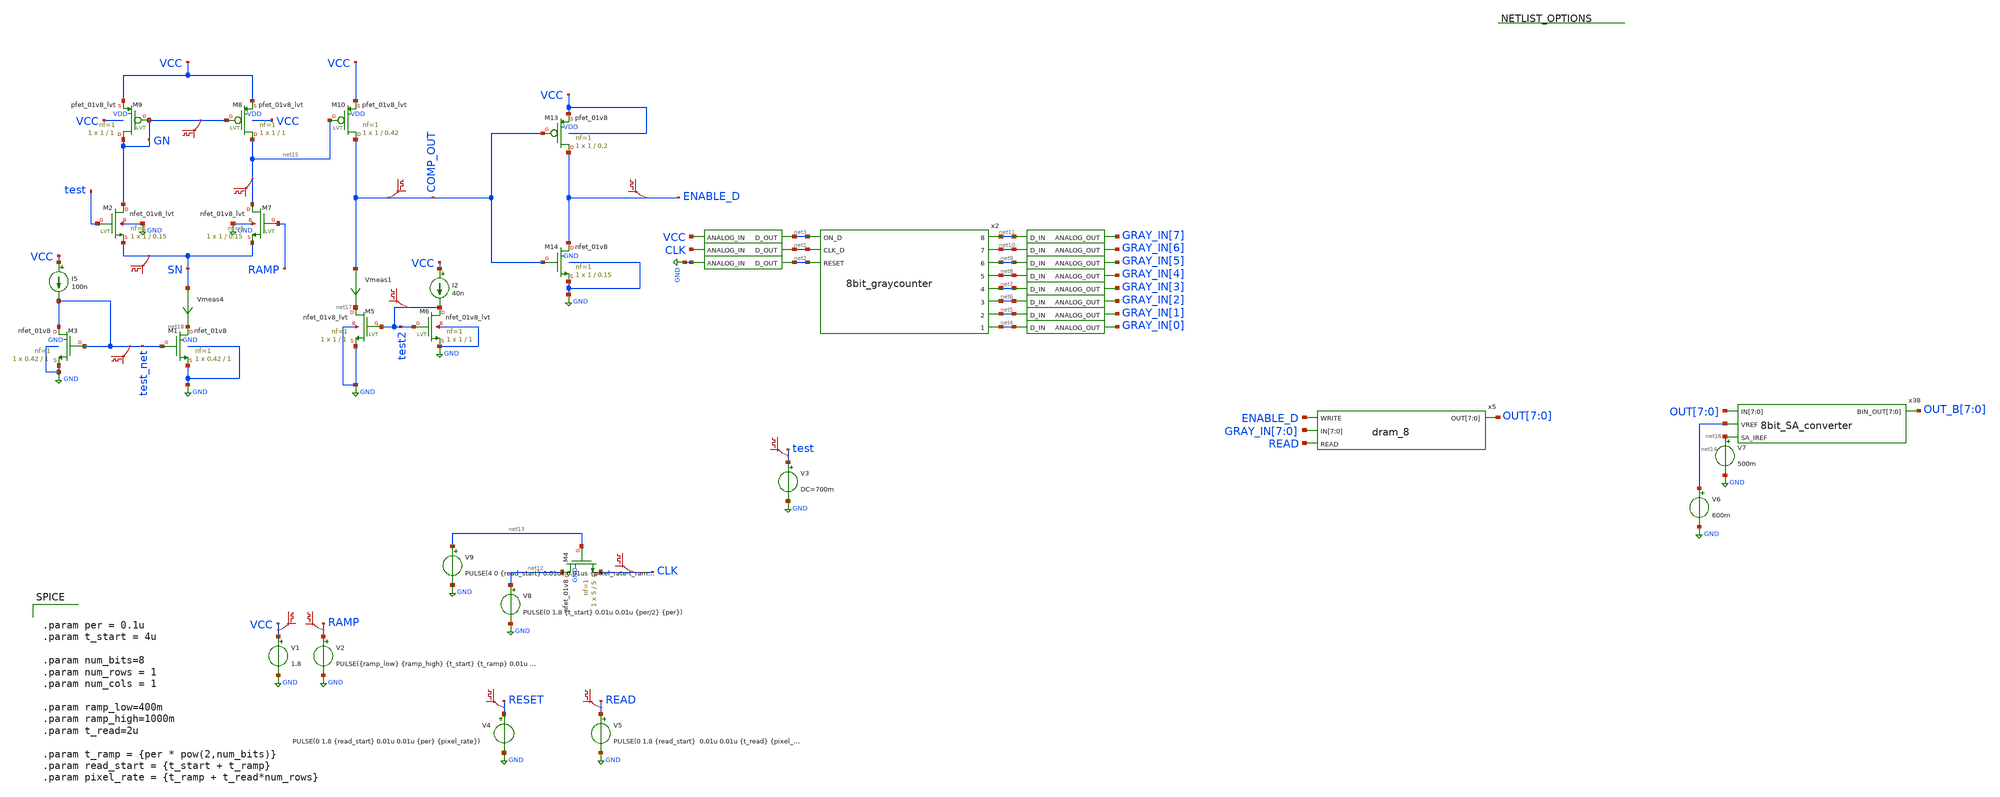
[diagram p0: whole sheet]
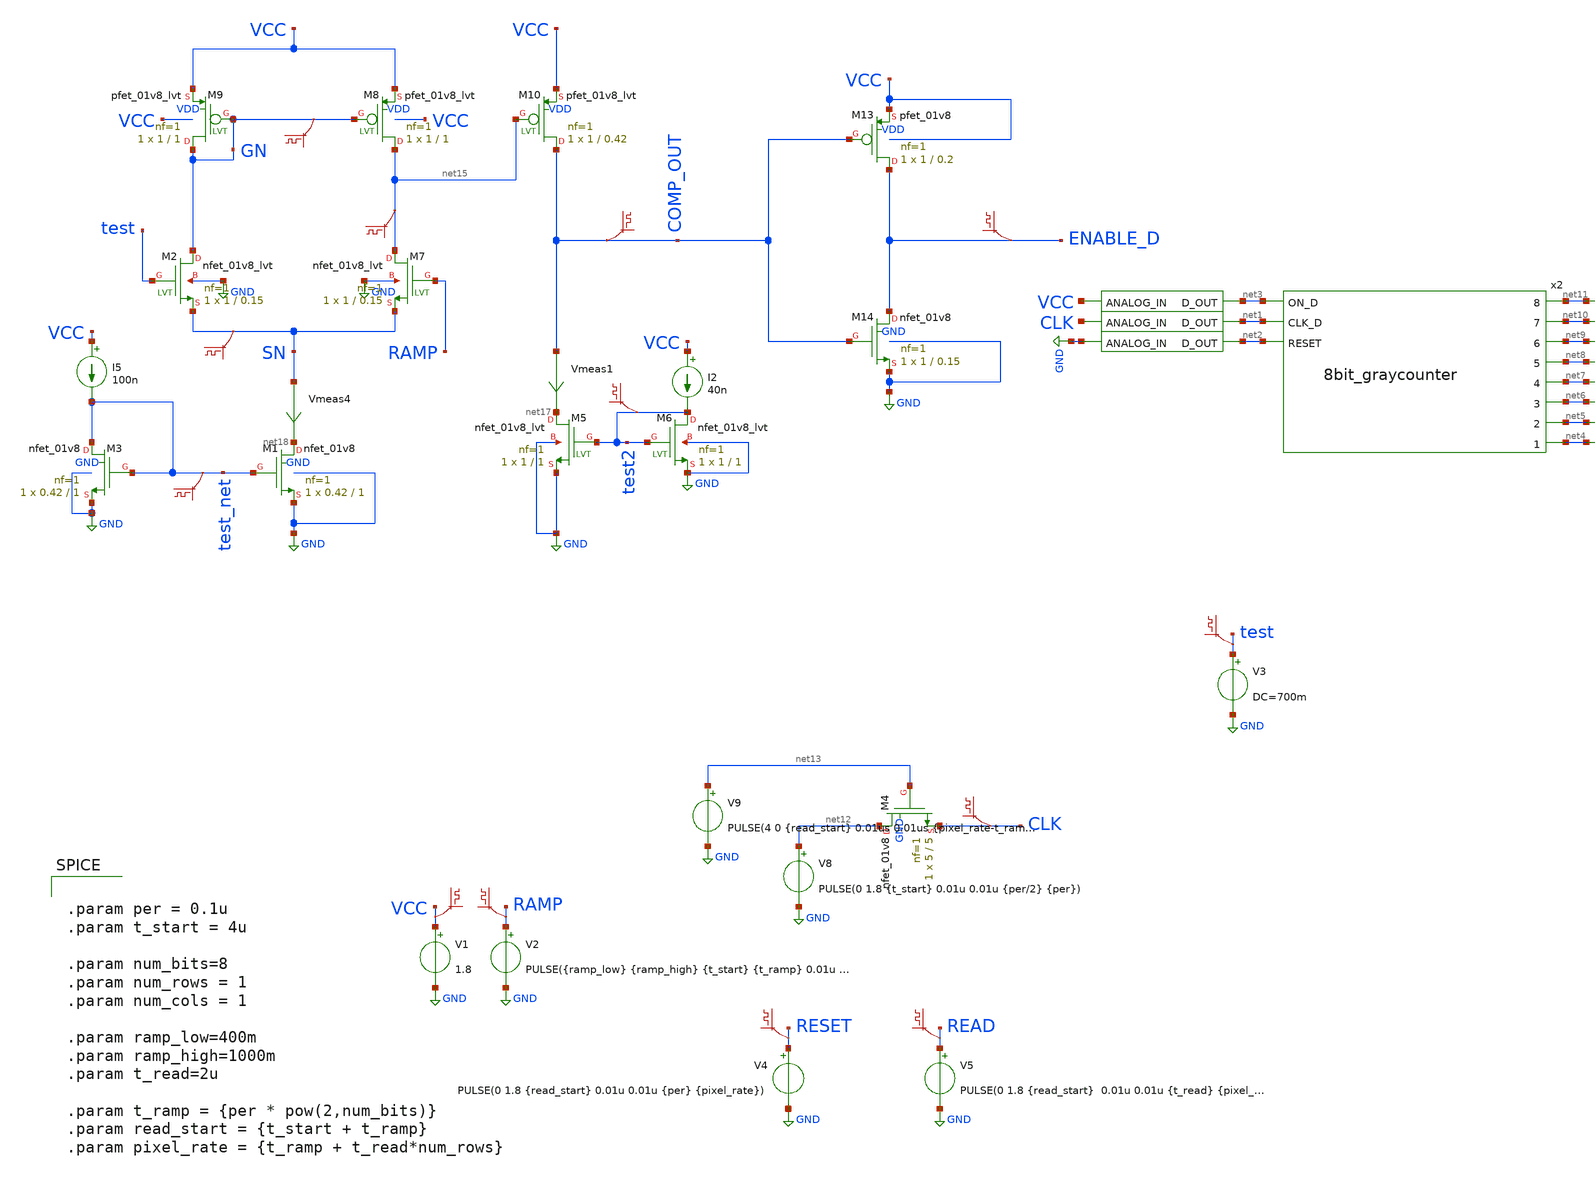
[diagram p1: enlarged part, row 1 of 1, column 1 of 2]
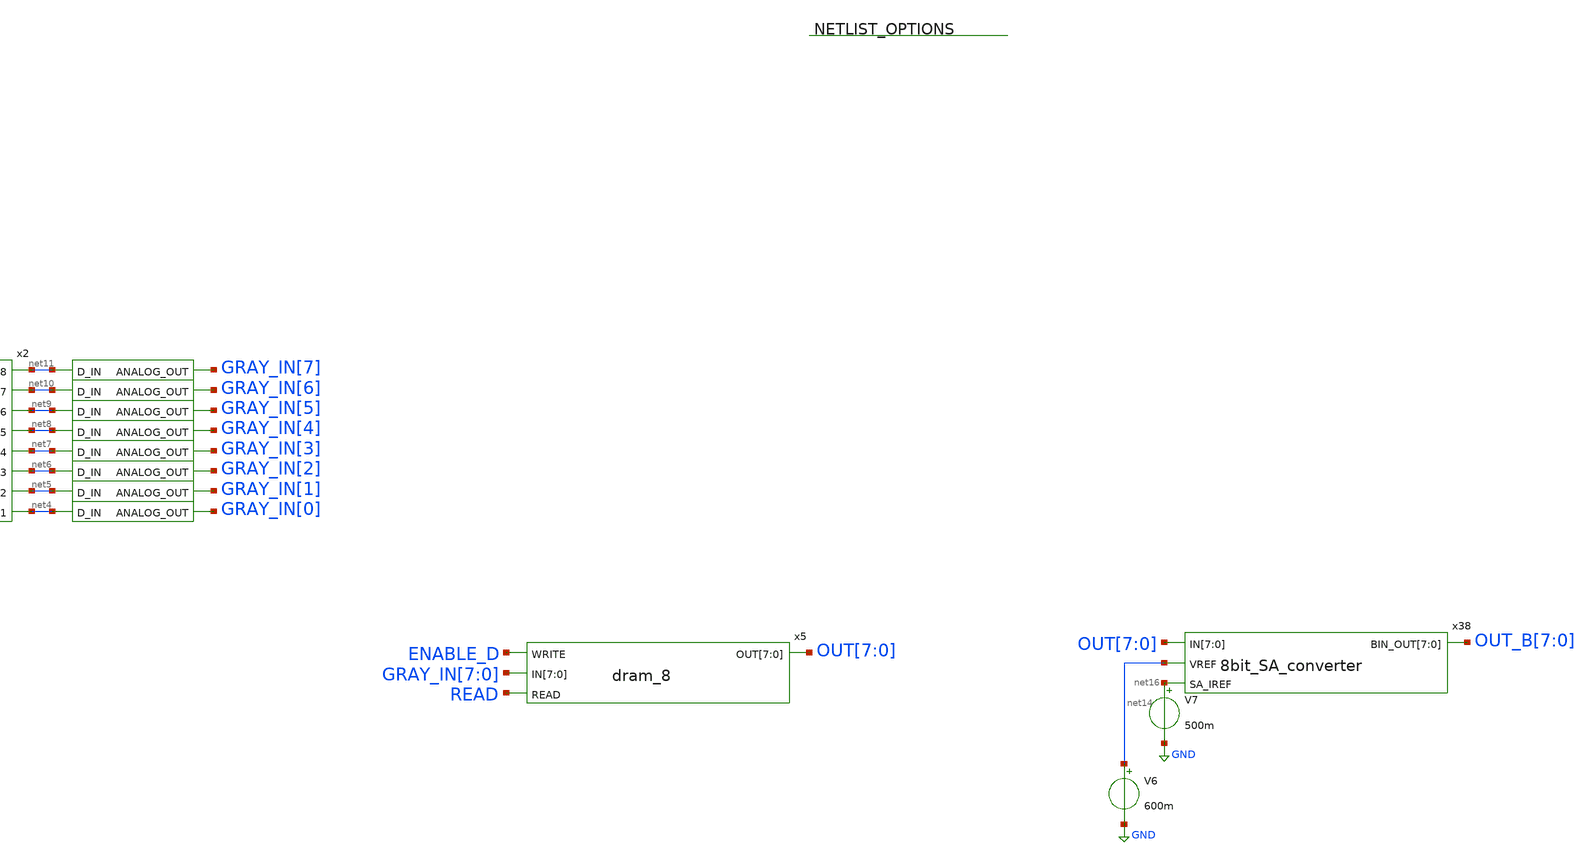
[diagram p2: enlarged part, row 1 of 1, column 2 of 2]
** sch_path: xschem/testbench/adc_testbench.sch
**.subckt adc_testbench
V3 test GND DC=700m
x1 net2 GND adc_bridge
x3 net3 VCC adc_bridge
x4 net1 CLK adc_bridge
x2 net11 net3 net10 net1 net9 net8 net2 net7 net6 net5 net4 8bit_graycounter
V1 VCC GND 1.8
V2 RAMP GND PULSE({ramp_low} {ramp_high} {t_start} {t_ramp} 0.01u {pixel_rate-t_ramp} {pixel_rate})
.save v(ramp)
.save v(vcc)
V4 RESET GND PULSE(0 1.8 {read_start} 0.01u 0.01u {per} {pixel_rate})
.save v(reset)
V5 READ GND PULSE(0 1.8 {read_start} 0.01u 0.01u {t_read} {pixel_rate})
.save v(read)
V8 net12 GND PULSE(0 1.8 {t_start} 0.01u 0.01u {per/2} {per})
XM4 net12 net13 CLK GND sky130_fd_pr__nfet_01v8 L=5 W=5 nf=1 ad='int((nf+1)/2) * W/nf * 0.29' as='int((nf+2)/2) * W/nf * 0.29'
+ pd='2*int((nf+1)/2) * (W/nf + 0.29)' ps='2*int((nf+2)/2) * (W/nf + 0.29)' nrd='0.29 / W' nrs='0.29 / W'
+ sa=0 sb=0 sd=0 mult=1 m=1
V9 net13 GND PULSE(4 0 {read_start} 0.01us 0.01us {pixel_rate-t_ramp} {pixel_rate})
.save v(clk)
V6 net14 GND 600m
x38 OUT[7] OUT[6] OUT[5] OUT[4] OUT[3] OUT[2] OUT[1] OUT[0] net14 net16 OUT_B[7] OUT_B[6] OUT_B[5]
+ OUT_B[4] OUT_B[3] OUT_B[2] OUT_B[1] OUT_B[0] 8bit_SA_converter
.save v(test)
XM2 GN test SN GND sky130_fd_pr__nfet_01v8_lvt L=0.15 W=1 nf=1 ad='int((nf+1)/2) * W/nf * 0.29' as='int((nf+2)/2) * W/nf * 0.29'
+ pd='2*int((nf+1)/2) * (W/nf + 0.29)' ps='2*int((nf+2)/2) * (W/nf + 0.29)' nrd='0.29 / W' nrs='0.29 / W'
+ sa=0 sb=0 sd=0 mult=1 m=1
XM7 net15 RAMP SN GND sky130_fd_pr__nfet_01v8_lvt L=0.15 W=1 nf=1 ad='int((nf+1)/2) * W/nf * 0.29' as='int((nf+2)/2) * W/nf * 0.29'
+ pd='2*int((nf+1)/2) * (W/nf + 0.29)' ps='2*int((nf+2)/2) * (W/nf + 0.29)' nrd='0.29 / W' nrs='0.29 / W'
+ sa=0 sb=0 sd=0 mult=1 m=1
XM8 net15 GN VCC VDD sky130_fd_pr__pfet_01v8_lvt L=1 W=1 nf=1 ad='int((nf+1)/2) * W/nf * 0.29' as='int((nf+2)/2) * W/nf * 0.29'
+ pd='2*int((nf+1)/2) * (W/nf + 0.29)' ps='2*int((nf+2)/2) * (W/nf + 0.29)' nrd='0.29 / W' nrs='0.29 / W'
+ sa=0 sb=0 sd=0 mult=1 m=1
XM9 GN GN VCC VDD sky130_fd_pr__pfet_01v8_lvt L=1 W=1 nf=1 ad='int((nf+1)/2) * W/nf * 0.29' as='int((nf+2)/2) * W/nf * 0.29'
+ pd='2*int((nf+1)/2) * (W/nf + 0.29)' ps='2*int((nf+2)/2) * (W/nf + 0.29)' nrd='0.29 / W' nrs='0.29 / W'
+ sa=0 sb=0 sd=0 mult=1 m=1
XM10 COMP_OUT net15 VCC VDD sky130_fd_pr__pfet_01v8_lvt L=0.42 W=1 nf=1 ad='int((nf+1)/2) * W/nf * 0.29'
+ as='int((nf+2)/2) * W/nf * 0.29' pd='2*int((nf+1)/2) * (W/nf + 0.29)' ps='2*int((nf+2)/2) * (W/nf + 0.29)'
+ nrd='0.29 / W' nrs='0.29 / W' sa=0 sb=0 sd=0 mult=1 m=1
XM13 ENABLE_D COMP_OUT VCC VDD sky130_fd_pr__pfet_01v8 L=0.2 W=1 nf=1 ad='int((nf+1)/2) * W/nf * 0.29'
+ as='int((nf+2)/2) * W/nf * 0.29' pd='2*int((nf+1)/2) * (W/nf + 0.29)' ps='2*int((nf+2)/2) * (W/nf + 0.29)'
+ nrd='0.29 / W' nrs='0.29 / W' sa=0 sb=0 sd=0 mult=1 m=1
XM14 ENABLE_D COMP_OUT GND GND sky130_fd_pr__nfet_01v8 L=0.15 W=1 nf=1 ad='int((nf+1)/2) * W/nf * 0.29'
+ as='int((nf+2)/2) * W/nf * 0.29' pd='2*int((nf+1)/2) * (W/nf + 0.29)' ps='2*int((nf+2)/2) * (W/nf + 0.29)'
+ nrd='0.29 / W' nrs='0.29 / W' sa=0 sb=0 sd=0 mult=1 m=1
.save v(enable_d)
x5 OUT[7] OUT[6] OUT[5] OUT[4] OUT[3] OUT[2] OUT[1] OUT[0] ENABLE_D GRAY_IN[7] GRAY_IN[6] GRAY_IN[5]
+ GRAY_IN[4] GRAY_IN[3] GRAY_IN[2] GRAY_IN[1] GRAY_IN[0] READ dram_8
x16 GRAY_IN[7] net11 dac_bridge
x6 GRAY_IN[6] net10 dac_bridge
x7 GRAY_IN[5] net9 dac_bridge
x8 GRAY_IN[4] net8 dac_bridge
x9 GRAY_IN[3] net7 dac_bridge
x10 GRAY_IN[2] net6 dac_bridge
x11 GRAY_IN[1] net5 dac_bridge
x12 GRAY_IN[0] net4 dac_bridge
XM5 net17 test2 GND GND sky130_fd_pr__nfet_01v8_lvt L=1 W=1 nf=1 ad='int((nf+1)/2) * W/nf * 0.29' as='int((nf+2)/2) * W/nf * 0.29'
+ pd='2*int((nf+1)/2) * (W/nf + 0.29)' ps='2*int((nf+2)/2) * (W/nf + 0.29)' nrd='0.29 / W' nrs='0.29 / W'
+ sa=0 sb=0 sd=0 mult=1 m=1
I2 VCC test2 40n
XM6 test2 test2 GND GND sky130_fd_pr__nfet_01v8_lvt L=1 W=1 nf=1 ad='int((nf+1)/2) * W/nf * 0.29' as='int((nf+2)/2) * W/nf * 0.29'
+ pd='2*int((nf+1)/2) * (W/nf + 0.29)' ps='2*int((nf+2)/2) * (W/nf + 0.29)' nrd='0.29 / W' nrs='0.29 / W'
+ sa=0 sb=0 sd=0 mult=1 m=1
.save v(test2)
Vmeas1 COMP_OUT net17 0
.save i(vmeas1)
.save v(comp_out)
.save v(sn)
.save v(gn)
.save v(net15)
Vmeas4 SN net18 0
.save i(vmeas4)
I5 VCC test_net 100n
XM1 net18 test_net GND GND sky130_fd_pr__nfet_01v8 L=1 W=0.42 nf=1 ad='int((nf+1)/2) * W/nf * 0.29' as='int((nf+2)/2) * W/nf * 0.29'
+ pd='2*int((nf+1)/2) * (W/nf + 0.29)' ps='2*int((nf+2)/2) * (W/nf + 0.29)' nrd='0.29 / W' nrs='0.29 / W'
+ sa=0 sb=0 sd=0 mult=1 m=1
XM3 test_net test_net GND GND sky130_fd_pr__nfet_01v8 L=1 W=0.42 nf=1 ad='int((nf+1)/2) * W/nf * 0.29'
+ as='int((nf+2)/2) * W/nf * 0.29' pd='2*int((nf+1)/2) * (W/nf + 0.29)' ps='2*int((nf+2)/2) * (W/nf + 0.29)'
+ nrd='0.29 / W' nrs='0.29 / W' sa=0 sb=0 sd=0 mult=1 m=1
.save v(test_net)
V7 net16 GND 500m
**** begin user architecture code

** opencircuitdesign pdks install
.lib $::SKYWATER_MODELS/sky130.lib.spice tt




.param per = 0.1u
.param t_start = 4u

.param num_bits=8
.param num_rows = 1
.param num_cols = 1

.param ramp_low=400m
.param ramp_high=1000m
.param t_read=2u

.param t_ramp = {per * pow(2,num_bits)}
.param read_start = {t_start + t_ramp}
.param pixel_rate = {t_ramp + t_read*num_rows}


**** end user architecture code
**.ends

* expanding   symbol:  digital_prims/adc_bridge.sym # of pins=2
** sym_path: xschem/digital_prims/adc_bridge.sym
** sch_path: xschem/digital_prims/adc_bridge.sch
.subckt adc_bridge D_OUT ANALOG_IN
*.ipin ANALOG_IN
*.opin D_OUT
**** begin user architecture code


abridge [ANALOG_IN] [D_OUT] adc_buff
.model adc_buff adc_bridge(in_low=0.9 in_high =0.9)


**** end user architecture code
.ends


* expanding   symbol:  adc/8bit_graycounter.sym # of pins=11
** sym_path: xschem/adc/8bit_graycounter.sym
** sch_path: xschem/adc/8bit_graycounter.sch
.subckt 8bit_graycounter 8 ON_D 7 CLK_D 6 5 RESET 4 3 2 1
*.ipin ON_D
*.ipin CLK_D
*.ipin RESET
*.opin 7
*.opin 6
*.opin 5
*.opin 4
*.opin 3
*.opin 2
*.opin 1
*.opin 8
**** begin user architecture code


a1 [ON_D] CLK_D RESET [8 7 6 5 4 3 2 1] gc_sm
.model gc_sm d_state(state_file="/home/hni/topmetal_dps/xschem/adc/graycntr.in")


**** end user architecture code
.ends


* expanding   symbol:  8bit_SA_converter.sym # of pins=4
** sym_path: xschem/8bit_SA_converter.sym
** sch_path: xschem/8bit_SA_converter.sch
.subckt 8bit_SA_converter IN[7] IN[6] IN[5] IN[4] IN[3] IN[2] IN[1] IN[0] VREF SA_IREF BIN_OUT[7]
+ BIN_OUT[6] BIN_OUT[5] BIN_OUT[4] BIN_OUT[3] BIN_OUT[2] BIN_OUT[1] BIN_OUT[0]
*.ipin IN[7],IN[6],IN[5],IN[4],IN[3],IN[2],IN[1],IN[0]
*.ipin VREF
*.opin BIN_OUT[7],BIN_OUT[6],BIN_OUT[5],BIN_OUT[4],BIN_OUT[3],BIN_OUT[2],BIN_OUT[1],BIN_OUT[0]
*.ipin SA_IREF
x38 IN[7] IN[6] IN[5] IN[4] IN[3] IN[2] IN[1] IN[0] VREF SA_IREF OUT_A[7] OUT_A[6] OUT_A[5] OUT_A[4]
+ OUT_A[3] OUT_A[2] OUT_A[1] OUT_A[0] 8bit_SA
x11 net8 net9 net10 net7 net6 net11 net5 net12 net13 net4 net3 net14 net15 net2 net16 net1
+ 8bitgray2bin
x12 BIN_OUT[7] net8 dac_bridge
x13 BIN_OUT[6] net7 dac_bridge
x14 BIN_OUT[5] net6 dac_bridge
x16 BIN_OUT[4] net5 dac_bridge
x17 BIN_OUT[3] net4 dac_bridge
x18 BIN_OUT[2] net3 dac_bridge
x19 BIN_OUT[1] net2 dac_bridge
x37 BIN_OUT[0] net1 dac_bridge
x39 net9 OUT_A[7] adc_bridge
x40 net10 OUT_A[6] adc_bridge
x41 net11 OUT_A[5] adc_bridge
x42 net12 OUT_A[4] adc_bridge
x43 net13 OUT_A[3] adc_bridge
x44 net14 OUT_A[2] adc_bridge
x45 net15 OUT_A[1] adc_bridge
x46 net16 OUT_A[0] adc_bridge
.save v(bin_out[7])
.save v(bin_out[6])
.save v(bin_out[5])
.save v(bin_out[4])
.save v(bin_out[3])
.save v(bin_out[2])
.save v(bin_out[1])
.save v(bin_out[0])
.ends


* expanding   symbol:  digital_prims/dram_8.sym # of pins=4
** sym_path: xschem/digital_prims/dram_8.sym
** sch_path: xschem/digital_prims/dram_8.sch
.subckt dram_8 OUT[7] OUT[6] OUT[5] OUT[4] OUT[3] OUT[2] OUT[1] OUT[0] WRITE IN[7] IN[6] IN[5] IN[4]
+ IN[3] IN[2] IN[1] IN[0] READ
*.opin OUT[7],OUT[6],OUT[5],OUT[4],OUT[3],OUT[2],OUT[1],OUT[0]
*.ipin WRITE
*.ipin IN[7],IN[6],IN[5],IN[4],IN[3],IN[2],IN[1],IN[0]
*.ipin READ
x5 WRITE OUT[7] net8 IN[7] READ net8 dram
x6 WRITE OUT[6] net7 IN[6] READ net7 dram
x7 WRITE OUT[5] net6 IN[5] READ net6 dram
x25 WRITE OUT[4] net5 IN[4] READ net5 dram
x26 WRITE OUT[3] net4 IN[3] READ net4 dram
x27 WRITE OUT[2] net3 IN[2] READ net3 dram
x33 WRITE OUT[1] net2 IN[0] READ net2 dram
x34 WRITE OUT[0] net1 IN[1] READ net1 dram
.ends


* expanding   symbol:  digital_prims/dac_bridge.sym # of pins=2
** sym_path: xschem/digital_prims/dac_bridge.sym
** sch_path: xschem/digital_prims/dac_bridge.sch
.subckt dac_bridge ANALOG_OUT D_IN
*.ipin D_IN
*.opin ANALOG_OUT
**** begin user architecture code


abridge_d [D_IN] [ANALOG_OUT] dac_buff
.model dac_buff dac_bridge(out_high=1.8)


**** end user architecture code
.ends


* expanding   symbol:  8bit_SA.sym # of pins=4
** sym_path: xschem/8bit_SA.sym
** sch_path: xschem/8bit_SA.sch
.subckt 8bit_SA IN[7] IN[6] IN[5] IN[4] IN[3] IN[2] IN[1] IN[0] VREF SA_IREF OUT[7] OUT[6] OUT[5]
+ OUT[4] OUT[3] OUT[2] OUT[1] OUT[0]
*.ipin IN[7],IN[6],IN[5],IN[4],IN[3],IN[2],IN[1],IN[0]
*.ipin VREF
*.opin OUT[7],OUT[6],OUT[5],OUT[4],OUT[3],OUT[2],OUT[1],OUT[0]
*.ipin SA_IREF
x2 OUT[7] VREF IN[7] SA_IREF sens_amp
x3 OUT[6] VREF IN[6] SA_IREF sens_amp
x4 OUT[5] VREF IN[5] SA_IREF sens_amp
x5 OUT[4] VREF IN[4] SA_IREF sens_amp
x6 OUT[3] VREF IN[3] SA_IREF sens_amp
x7 OUT[2] net1 IN[2] SA_IREF sens_amp
x8 OUT[1] VREF IN[1] SA_IREF sens_amp
x9 OUT[0] VREF IN[0] SA_IREF sens_amp
.ends


* expanding   symbol:  adc/8bitgray2bin.sym # of pins=16
** sym_path: xschem/adc/8bitgray2bin.sym
** sch_path: xschem/adc/8bitgray2bin.sch
.subckt 8bitgray2bin 8 g8 g7 7 6 g6 5 g5 g4 4 3 g3 g2 2 g1 1
*.opin 7
*.opin 6
*.opin 5
*.opin 4
*.opin 3
*.opin 2
*.opin 1
*.opin 8
*.ipin g5
*.ipin g4
*.ipin g3
*.ipin g8
*.ipin g7
*.ipin g6
*.ipin g2
*.ipin g1
**** begin user architecture code


* lsb first.
a1 [g1 g2 g3 g4 g5 g6 g7 g8] [1 2 3 4 5 6 7 8] gray2bin_lut
.model gray2bin_lut d_genlut(rise_delay=[1p 1p] fall_delay=[1p 1p]  input_load=[1p 1p]
+ input_delay=[0 0]
+ table_values=01101001100101101001011001101001100101100110100101101001100101101001011001101001011010011001011001101001100101101001011001101001100101100110100101101001100101100110100110010110100101100110100101101001100101101001011001101001100101100110100101101001100101100011110011000011110000110011110011000011001111000011110011000011110000110011110000111100110000110011110011000011110000110011110011000011001111000011110011000011001111001100001111000011001111000011110011000011110000110011110011000011001111000011110011000011000011111111000011110000000011111111000000001111000011111111000011110000000011110000111111110000000011111111000011110000000011111111000000001111000011111111000000001111111100001111000000001111000011111111000011110000000011111111000000001111000011111111000000000000111111111111111100000000111111110000000000000000111111111111111100000000000000001111111100000000111111111111111100000000111111110000000000000000111111110000000011111111111111110000000000000000111111111111111100000000111111110000000000000000111111110000000000000000111111111111111111111111111111110000000000000000111111111111111100000000000000000000000000000000111111111111111111111111111111110000000000000000000000000000000011111111111111110000000000000000111111111111111111111111111111110000000000000000000000000000000000000000000000001111111111111111111111111111111111111111111111111111111111111111000000000000000000000000000000001111111111111111111111111111111100000000000000000000000000000000000000000000000000000000000000001111111111111111111111111111111100000000000000000000000000000000000000000000000000000000000000001111111111111111111111111111111111111111111111111111111111111111111111111111111111111111111111111111111111111111111111111111111100000000000000000000000000000000000000000000000000000000000000000000000000000000000000000000000000000000000000000000000000000000000000000000000000000000000000000000000000000000000000000000000011111111111111111111111111111111111111111111111111111111111111111111111111111111111111111111111111111111111111111111111111111111)




**** end user architecture code
.ends


* expanding   symbol:  digital_prims/dram.sym # of pins=6
** sym_path: xschem/digital_prims/dram.sym
** sch_path: xschem/digital_prims/dram.sch
.subckt dram WWL RBL storage WBL RWL GND
*.opin RBL
*.ipin RWL
*.ipin WBL
*.ipin WWL
*.opin storage
*.ipin GND
XM3 RWL storage RBL GND sky130_fd_pr__nfet_01v8 L=0.15 W=1 nf=1 ad='int((nf+1)/2) * W/nf * 0.29' as='int((nf+2)/2) * W/nf * 0.29'
+ pd='2*int((nf+1)/2) * (W/nf + 0.29)' ps='2*int((nf+2)/2) * (W/nf + 0.29)' nrd='0.29 / W' nrs='0.29 / W'
+ sa=0 sb=0 sd=0 mult=1 m=1
XM1 WBL WWL storage GND sky130_fd_pr__nfet_01v8 L=0.15 W=1 nf=1 ad='int((nf+1)/2) * W/nf * 0.29' as='int((nf+2)/2) * W/nf * 0.29'
+ pd='2*int((nf+1)/2) * (W/nf + 0.29)' ps='2*int((nf+2)/2) * (W/nf + 0.29)' nrd='0.29 / W' nrs='0.29 / W'
+ sa=0 sb=0 sd=0 mult=1 m=1
.ends


* expanding   symbol:  sens_amp.sym # of pins=4
** sym_path: xschem/sens_amp.sym
** sch_path: xschem/sens_amp.sch
.subckt sens_amp OUT REF V_IN SA_IREF
*.ipin REF
*.ipin V_IN
*.opin OUT
*.ipin SA_IREF
XM5 net1 GN VDD VDD sky130_fd_pr__pfet_01v8_lvt L=0.5 W=1 nf=1 ad='W * 0.29' as='W * 0.29' pd='2*(W + 0.29)'
+ ps='2*(W + 0.29)' nrd=0 nrs=0 sa=0 sb=0 sd=0 mult=1 m=1
XM6 GN GN VDD VDD sky130_fd_pr__pfet_01v8_lvt L=0.5 W=1 nf=1 ad='W * 0.29' as='W * 0.29' pd='2*(W + 0.29)'
+ ps='2*(W + 0.29)' nrd=0 nrs=0 sa=0 sb=0 sd=0 mult=1 m=1
XM23 net1 V_IN net2 GND sky130_fd_pr__nfet_01v8_lvt L=0.15 W=4 nf=1 ad='W * 0.29' as='W * 0.29' pd='2*(W + 0.29)'
+ ps='2*(W + 0.29)' nrd=0 nrs=0 sa=0 sb=0 sd=0 mult=1 m=1
XM16 GN REF net2 GND sky130_fd_pr__nfet_01v8_lvt L=0.15 W=4 nf=1 ad='W * 0.29' as='W * 0.29' pd='2*(W + 0.29)'
+ ps='2*(W + 0.29)' nrd=0 nrs=0 sa=0 sb=0 sd=0 mult=1 m=1
XM1 OUT net1 GND GND sky130_fd_pr__nfet_01v8_lvt L=0.15 W=1 nf=1 ad='W * 0.29' as='W * 0.29' pd='2*(W + 0.29)'
+ ps='2*(W + 0.29)' nrd=0 nrs=0 sa=0 sb=0 sd=0 mult=1 m=1
XM2 OUT net1 VDD VDD sky130_fd_pr__pfet_01v8_lvt L=0.35 W=3 nf=1 ad='W * 0.29' as='W * 0.29' pd='2*(W + 0.29)'
+ ps='2*(W + 0.29)' nrd=0 nrs=0 sa=0 sb=0 sd=0 mult=1 m=1
XM3 net3 SA_IREF GND GND sky130_fd_pr__nfet_01v8_lvt L=1 W=0.5 nf=1 ad='W * 0.29' as='W * 0.29' pd='2*(W + 0.29)'
+ ps='2*(W + 0.29)' nrd=0 nrs=0 sa=0 sb=0 sd=0 mult=1 m=1
Vmeas net2 net3 0
.save i(vmeas)
.ends

.GLOBAL GND
**** begin user architecture code


.control
*dc v2 200m .8 0.0001
*plot v(test)
tran 0.1u 300u

plot v(SN)
write adc_testbench.raw
options filetype=ascii
write adc_testbench.out
.endc


**** end user architecture code
.end
